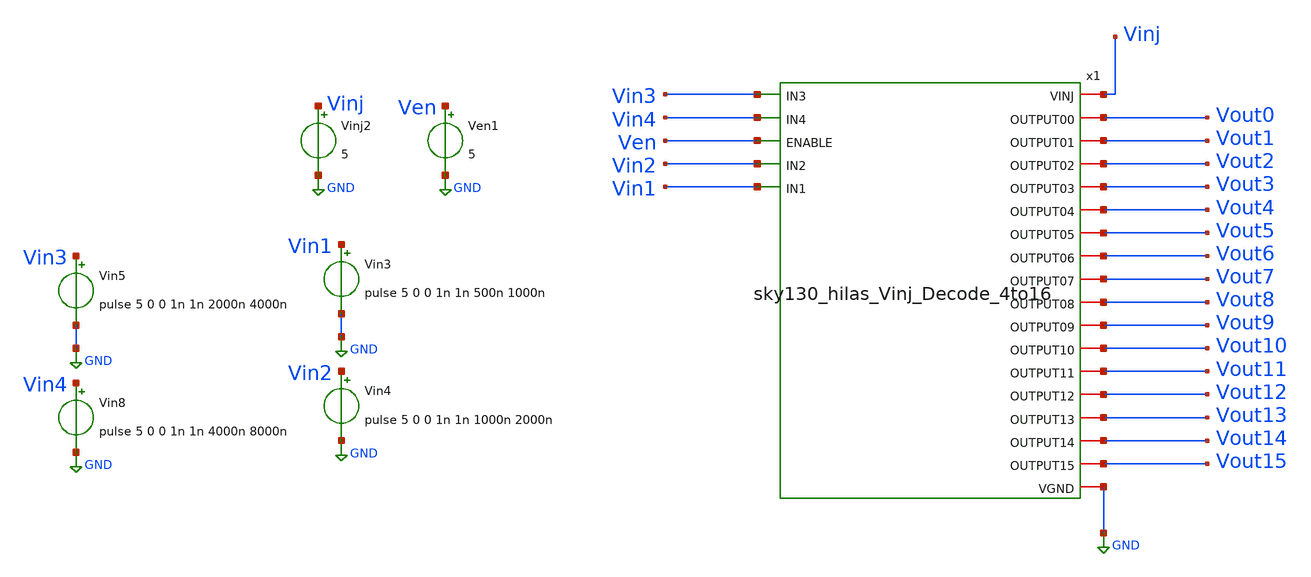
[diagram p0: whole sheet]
** sch_path: sky130_cells/RDAC/Sims/Vinj_Decode4to16_testbench.sch
**.subckt Vinj_Decode4to16_testbench
Vin3 Vin1 GND pulse 5 0 0 1n 1n 500n 1000n
Vin4 Vin2 GND pulse 5 0 0 1n 1n 1000n 2000n
Vinj2 Vinj GND 5
Ven1 Ven GND 5
Vin5 Vin3 GND pulse 5 0 0 1n 1n 2000n 4000n
Vin8 Vin4 GND pulse 5 0 0 1n 1n 4000n 8000n
x1 Vinj Vout0 Vout1 Vout2 Vout3 Vin3 Vin4 Vout4 Vout5 Vout6 Vout7 Ven Vin2 Vin1 Vout8 Vout9 Vout10
+ Vout11 Vout12 Vout13 Vout14 Vout15 GND sky130_hilas_Vinj_Decode_4to16
**** begin user architecture code

** opencircuitdesign pdks install
.lib $::SKYWATER_MODELS/sky130.lib.spice tt




.control
	tran 0.5n 8000n
	plot V(Vin1) V(Vin2) title 'Decoder Inputs'
	plot V(Vout0) V(Vout2) V(Vout4) V(Vout6) V(Vout8) V(Vout10) V(Vout12) V(Vout14) title 'Decoder Output'
	plot V(Vout1) V(Vout3) V(Vout5) V(Vout7) V(Vout9) V(Vout11) V(Vout13) V(Vout15) title 'Decoder Output'
.endc

.end

**** end user architecture code
**.ends

* expanding   symbol:  sky130_cells/RDAC/Design/sky130_hilas_Vinj_Decode_4to16.sym # of pins=23
** sym_path: sky130_cells/RDAC/Design/sky130_hilas_Vinj_Decode_4to16.sym
** sch_path: sky130_cells/RDAC/Design/sky130_hilas_Vinj_Decode_4to16.sch
.subckt sky130_hilas_Vinj_Decode_4to16 VINJ OUTPUT00 OUTPUT01 OUTPUT02 OUTPUT03 IN3 IN4 OUTPUT04
+ OUTPUT05 OUTPUT06 OUTPUT07 ENABLE IN2 IN1 OUTPUT08 OUTPUT09 OUTPUT10 OUTPUT11 OUTPUT12 OUTPUT13 OUTPUT14
+ OUTPUT15 VGND
*.ipin ENABLE
*.ipin IN1
*.ipin IN2
*.ipin IN3
*.ipin IN4
*.iopin VGND
*.iopin OUTPUT00
*.iopin OUTPUT01
*.iopin OUTPUT02
*.iopin OUTPUT03
*.iopin OUTPUT04
*.iopin OUTPUT05
*.iopin OUTPUT06
*.iopin OUTPUT07
*.iopin OUTPUT08
*.iopin OUTPUT09
*.iopin OUTPUT10
*.iopin OUTPUT11
*.iopin OUTPUT12
*.iopin OUTPUT13
*.iopin OUTPUT14
*.iopin OUTPUT15
*.iopin VINJ
x1 VINJ ENABLE ENABLE IN4 net1 net2 net3 net4 VGND sky130_hilas_VinjDecode2to4
x2 VINJ net1 net1 IN2 OUTPUT00 OUTPUT01 OUTPUT02 OUTPUT03 VGND sky130_hilas_VinjDecode2to4
x3 VINJ net2 net2 IN2 OUTPUT04 OUTPUT05 OUTPUT06 OUTPUT07 VGND sky130_hilas_VinjDecode2to4
x4 VINJ net3 net3 IN2 OUTPUT08 OUTPUT09 OUTPUT10 OUTPUT11 VGND sky130_hilas_VinjDecode2to4
x5 VINJ net4 net4 IN2 OUTPUT12 OUTPUT13 OUTPUT14 OUTPUT15 VGND sky130_hilas_VinjDecode2to4
.ends


* expanding   symbol:  sky130_cells/RDAC/Design/sky130_hilas_VinjDecode2to4.sym # of pins=8
** sym_path: sky130_cells/RDAC/Design/sky130_hilas_VinjDecode2to4.sym
** sch_path: sky130_cells/RDAC/Design/sky130_hilas_VinjDecode2to4.sch
.subckt sky130_hilas_VinjDecode2to4 VINJ IN[1] IN[0] ENABLE OUTPUT00 OUTPUT01 OUTPUT10 OUTPUT11 VGND
*.ipin ENABLE
*.opin OUTPUT00
*.opin OUTPUT01
*.opin OUTPUT10
*.opin OUTPUT11
*.iopin VINJ
*.iopin VGND
*.ipin IN[1],IN[0]
x2 VINJ IN[1] VinjNOR3_2/Input2 VGND sky130_hilas_VinjInv2
x3 VINJ IN[0] VinjNOR3_1/Input1 VGND sky130_hilas_VinjInv2
x4 VINJ ENABLE VinjNOR3_3/Input3 VGND sky130_hilas_VinjInv2
x1 VINJ IN[1] IN[0] VinjNOR3_3/Input3 OUTPUT00 VGND sky130_hilas_VinjNOR3
x5 VINJ IN[1] VinjNOR3_1/Input1 VinjNOR3_3/Input3 OUTPUT01 VGND sky130_hilas_VinjNOR3
x6 VINJ VinjNOR3_2/Input2 IN[0] VinjNOR3_3/Input3 OUTPUT10 VGND sky130_hilas_VinjNOR3
x7 VINJ VinjNOR3_2/Input2 VinjNOR3_1/Input1 VinjNOR3_3/Input3 OUTPUT11 VGND sky130_hilas_VinjNOR3
.ends


* expanding   symbol:  sky130_cells/RDAC/Design/sky130_hilas_VinjInv2.sym # of pins=4
** sym_path: sky130_cells/RDAC/Design/sky130_hilas_VinjInv2.sym
** sch_path: sky130_cells/RDAC/Design/sky130_hilas_VinjInv2.sch
.subckt sky130_hilas_VinjInv2 Vinj Input Output GND
*.ipin Input
*.opin Output
*.iopin Vinj
*.iopin GND
XM4 Output Input Vinj Vinj sky130_fd_pr__pfet_g5v0d10v5 L=0.53 W=0.42 nf=1 ad='int((nf+1)/2) * W/nf * 0.29'
+ as='int((nf+2)/2) * W/nf * 0.29' pd='2*int((nf+1)/2) * (W/nf + 0.29)' ps='2*int((nf+2)/2) * (W/nf + 0.29)'
+ nrd='0.29 / W' nrs='0.29 / W' sa=0 sb=0 sd=0 mult=1 m=1
XM3 Output Input GND GND sky130_fd_pr__nfet_g5v0d10v5 L=0.52 W=0.42 nf=1 ad='int((nf+1)/2) * W/nf * 0.29'
+ as='int((nf+2)/2) * W/nf * 0.29' pd='2*int((nf+1)/2) * (W/nf + 0.29)' ps='2*int((nf+2)/2) * (W/nf + 0.29)'
+ nrd='0.29 / W' nrs='0.29 / W' sa=0 sb=0 sd=0 mult=1 m=1
.ends


* expanding   symbol:  sky130_cells/RDAC/Design/sky130_hilas_VinjNOR3.sym # of pins=6
** sym_path: sky130_cells/RDAC/Design/sky130_hilas_VinjNOR3.sym
** sch_path: sky130_cells/RDAC/Design/sky130_hilas_VinjNOR3.sch
.subckt sky130_hilas_VinjNOR3 Vinj Input1 Input2 Input3 OUTPUT GND
*.ipin Input3
*.ipin Input1
*.ipin Input2
*.iopin Vinj
*.iopin GND
*.opin OUTPUT
XM1 OUTPUT Input3 GND GND sky130_fd_pr__nfet_g5v0d10v5 L=0.5 W=0.42 nf=1 ad='int((nf+1)/2) * W/nf * 0.29'
+ as='int((nf+2)/2) * W/nf * 0.29' pd='2*int((nf+1)/2) * (W/nf + 0.29)' ps='2*int((nf+2)/2) * (W/nf + 0.29)'
+ nrd='0.29 / W' nrs='0.29 / W' sa=0 sb=0 sd=0 mult=1 m=1
XM2 OUTPUT Input1 GND GND sky130_fd_pr__nfet_g5v0d10v5 L=0.51 W=0.43 nf=1 ad='int((nf+1)/2) * W/nf * 0.29'
+ as='int((nf+2)/2) * W/nf * 0.29' pd='2*int((nf+1)/2) * (W/nf + 0.29)' ps='2*int((nf+2)/2) * (W/nf + 0.29)'
+ nrd='0.29 / W' nrs='0.29 / W' sa=0 sb=0 sd=0 mult=1 m=1
XM3 OUTPUT Input2 GND GND sky130_fd_pr__nfet_g5v0d10v5 L=0.5 W=0.42 nf=1 ad='int((nf+1)/2) * W/nf * 0.29'
+ as='int((nf+2)/2) * W/nf * 0.29' pd='2*int((nf+1)/2) * (W/nf + 0.29)' ps='2*int((nf+2)/2) * (W/nf + 0.29)'
+ nrd='0.29 / W' nrs='0.29 / W' sa=0 sb=0 sd=0 mult=1 m=1
XM6 OUTPUT Input2 net2 Vinj sky130_fd_pr__pfet_g5v0d10v5 L=0.52 W=0.43 nf=1 ad='int((nf+1)/2) * W/nf * 0.29'
+ as='int((nf+2)/2) * W/nf * 0.29' pd='2*int((nf+1)/2) * (W/nf + 0.29)' ps='2*int((nf+2)/2) * (W/nf + 0.29)'
+ nrd='0.29 / W' nrs='0.29 / W' sa=0 sb=0 sd=0 mult=1 m=1
XM4 net2 Input1 net1 Vinj sky130_fd_pr__pfet_g5v0d10v5 L=0.52 W=0.42 nf=1 ad='int((nf+1)/2) * W/nf * 0.29'
+ as='int((nf+2)/2) * W/nf * 0.29' pd='2*int((nf+1)/2) * (W/nf + 0.29)' ps='2*int((nf+2)/2) * (W/nf + 0.29)'
+ nrd='0.29 / W' nrs='0.29 / W' sa=0 sb=0 sd=0 mult=1 m=1
XM5 net1 Input3 Vinj Vinj sky130_fd_pr__pfet_g5v0d10v5 L=0.53 W=0.42 nf=1 ad='int((nf+1)/2) * W/nf * 0.29'
+ as='int((nf+2)/2) * W/nf * 0.29' pd='2*int((nf+1)/2) * (W/nf + 0.29)' ps='2*int((nf+2)/2) * (W/nf + 0.29)'
+ nrd='0.29 / W' nrs='0.29 / W' sa=0 sb=0 sd=0 mult=1 m=1
.ends

.GLOBAL GND
.end
